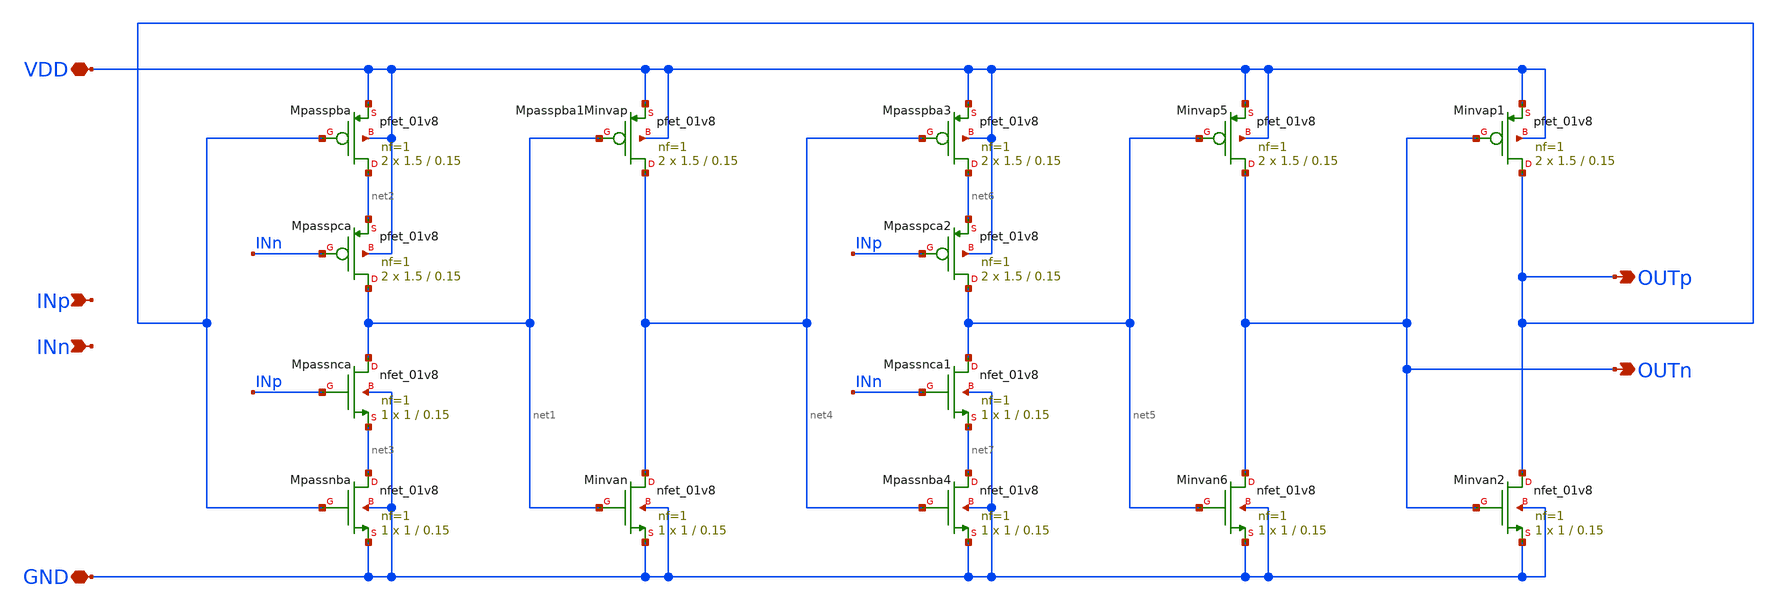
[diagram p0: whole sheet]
** sch_path: design/divider_ff/divider_ff.sch
**.subckt divider_ff INn OUTp VDD GND OUTn INp
*.ipin INn
*.opin OUTp
*.iopin VDD
*.iopin GND
*.opin OUTn
*.ipin INp
XMpasspba net2 OUTp VDD VDD sky130_fd_pr__pfet_01v8 L=0.15 W=1.5 nf=1 ad='W * 0.29' as='W * 0.29' pd='W + 2 * 0.29'
+ ps='W + 2 * 0.29' nrd=0 nrs=0 sa=0 sb=0 sd=0 mult=2 m=2
XMpasspca net1 INn net2 VDD sky130_fd_pr__pfet_01v8 L=0.15 W=1.5 nf=1 ad='W * 0.29' as='W * 0.29' pd='W + 2 * 0.29'
+ ps='W + 2 * 0.29' nrd=0 nrs=0 sa=0 sb=0 sd=0 mult=2 m=2
XMpasspba1Minvap net4 net1 VDD VDD sky130_fd_pr__pfet_01v8 L=0.15 W=1.5 nf=1 ad='W * 0.29' as='W * 0.29'
+ pd='W + 2 * 0.29' ps='W + 2 * 0.29' nrd=0 nrs=0 sa=0 sb=0 sd=0 mult=2 m=2
XMpasspba3 net6 net4 VDD VDD sky130_fd_pr__pfet_01v8 L=0.15 W=1.5 nf=1 ad='W * 0.29' as='W * 0.29' pd='W + 2 * 0.29'
+ ps='W + 2 * 0.29' nrd=0 nrs=0 sa=0 sb=0 sd=0 mult=2 m=2
XMpasspca2 net5 INp net6 VDD sky130_fd_pr__pfet_01v8 L=0.15 W=1.5 nf=1 ad='W * 0.29' as='W * 0.29' pd='W + 2 * 0.29'
+ ps='W + 2 * 0.29' nrd=0 nrs=0 sa=0 sb=0 sd=0 mult=2 m=2
XMinvap5 OUTn net5 VDD VDD sky130_fd_pr__pfet_01v8 L=0.15 W=1.5 nf=1 ad='W * 0.29' as='W * 0.29' pd='W + 2 * 0.29'
+ ps='W + 2 * 0.29' nrd=0 nrs=0 sa=0 sb=0 sd=0 mult=2 m=2
XMinvap1 OUTp OUTn VDD VDD sky130_fd_pr__pfet_01v8 L=0.15 W=1.5 nf=1 ad='W * 0.29' as='W * 0.29' pd='W + 2 * 0.29'
+ ps='W + 2 * 0.29' nrd=0 nrs=0 sa=0 sb=0 sd=0 mult=2 m=2
XMpassnca net1 INp net3 GND sky130_fd_pr__nfet_01v8 L=0.15 W=1 nf=1 ad='W * 0.29' as='W * 0.29' pd='W + 2 * 0.29'
+ ps='W + 2 * 0.29' nrd=0 nrs=0 sa=0 sb=0 sd=0 mult=1 m=1
XMpassnba net3 OUTp GND GND sky130_fd_pr__nfet_01v8 L=0.15 W=1 nf=1 ad='W * 0.29' as='W * 0.29' pd='W + 2 * 0.29'
+ ps='W + 2 * 0.29' nrd=0 nrs=0 sa=0 sb=0 sd=0 mult=1 m=1
XMinvan net4 net1 GND GND sky130_fd_pr__nfet_01v8 L=0.15 W=1 nf=1 ad='W * 0.29' as='W * 0.29' pd='W + 2 * 0.29'
+ ps='W + 2 * 0.29' nrd=0 nrs=0 sa=0 sb=0 sd=0 mult=1 m=1
XMpassnca1 net5 INn net7 GND sky130_fd_pr__nfet_01v8 L=0.15 W=1 nf=1 ad='W * 0.29' as='W * 0.29' pd='W + 2 * 0.29'
+ ps='W + 2 * 0.29' nrd=0 nrs=0 sa=0 sb=0 sd=0 mult=1 m=1
XMpassnba4 net7 net4 GND GND sky130_fd_pr__nfet_01v8 L=0.15 W=1 nf=1 ad='W * 0.29' as='W * 0.29' pd='W + 2 * 0.29'
+ ps='W + 2 * 0.29' nrd=0 nrs=0 sa=0 sb=0 sd=0 mult=1 m=1
XMinvan6 OUTn net5 GND GND sky130_fd_pr__nfet_01v8 L=0.15 W=1 nf=1 ad='W * 0.29' as='W * 0.29' pd='W + 2 * 0.29'
+ ps='W + 2 * 0.29' nrd=0 nrs=0 sa=0 sb=0 sd=0 mult=1 m=1
XMinvan2 OUTp OUTn GND GND sky130_fd_pr__nfet_01v8 L=0.15 W=1 nf=1 ad='W * 0.29' as='W * 0.29' pd='W + 2 * 0.29'
+ ps='W + 2 * 0.29' nrd=0 nrs=0 sa=0 sb=0 sd=0 mult=1 m=1
**.ends
.end
